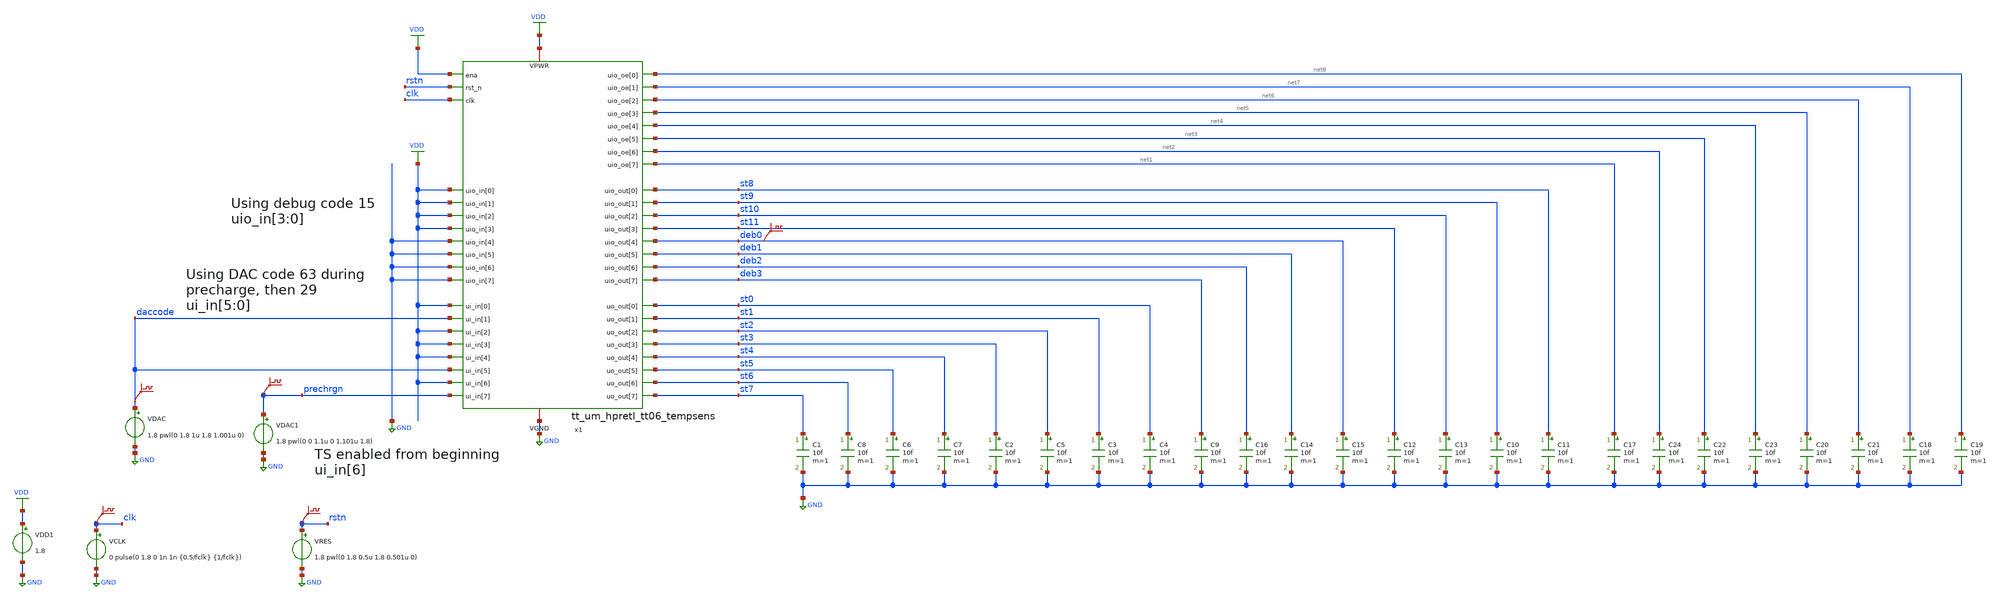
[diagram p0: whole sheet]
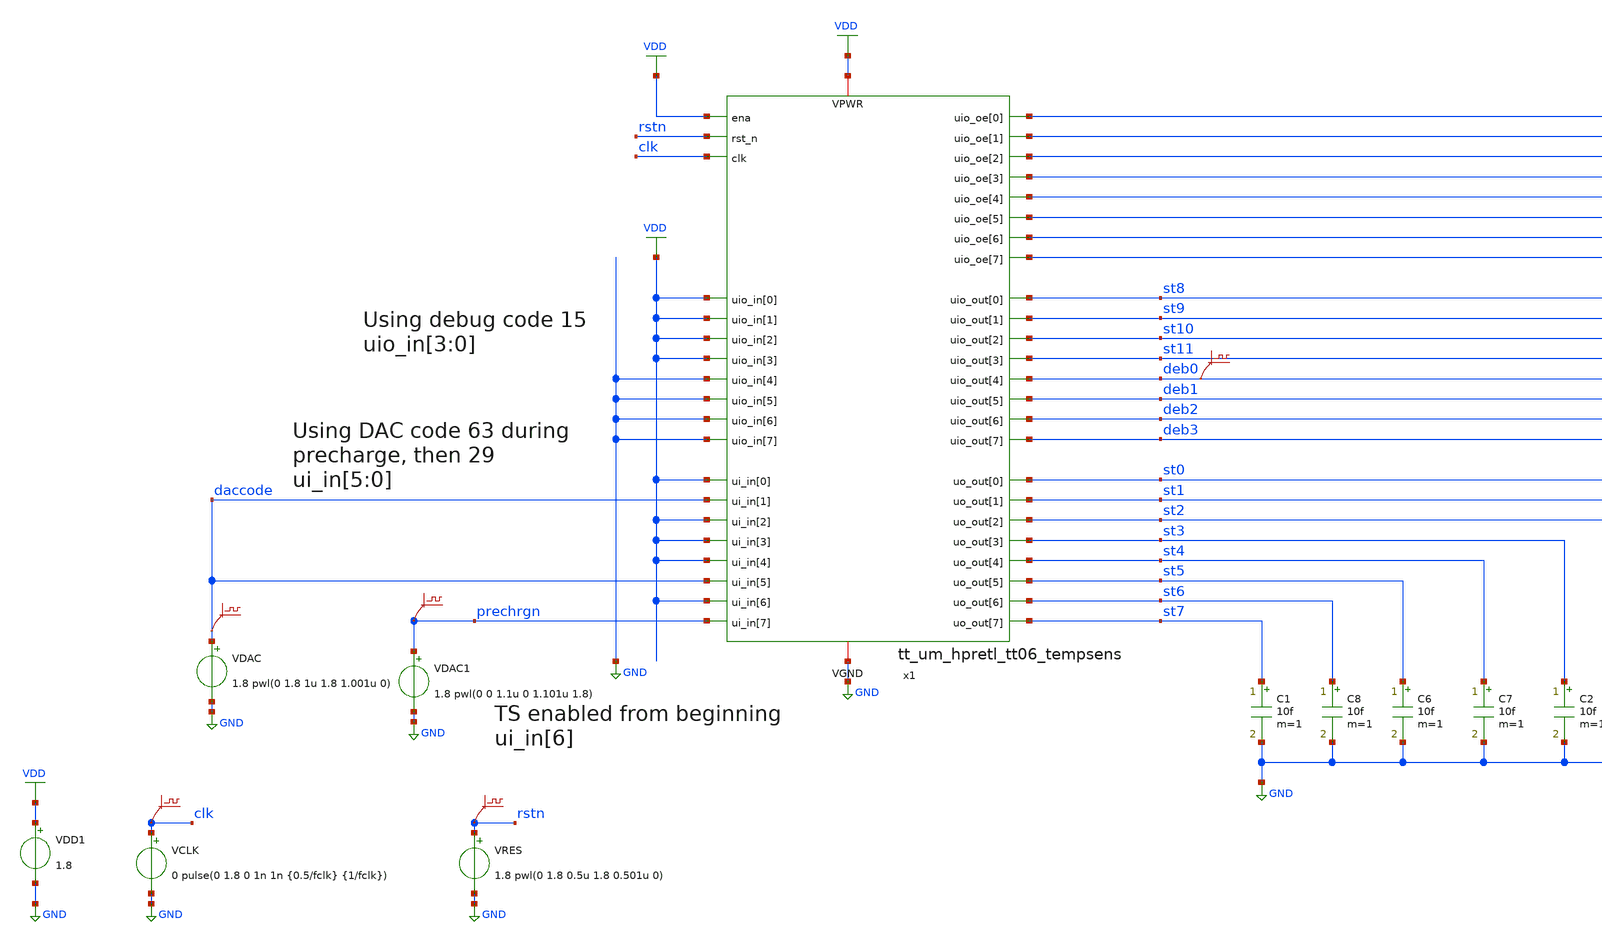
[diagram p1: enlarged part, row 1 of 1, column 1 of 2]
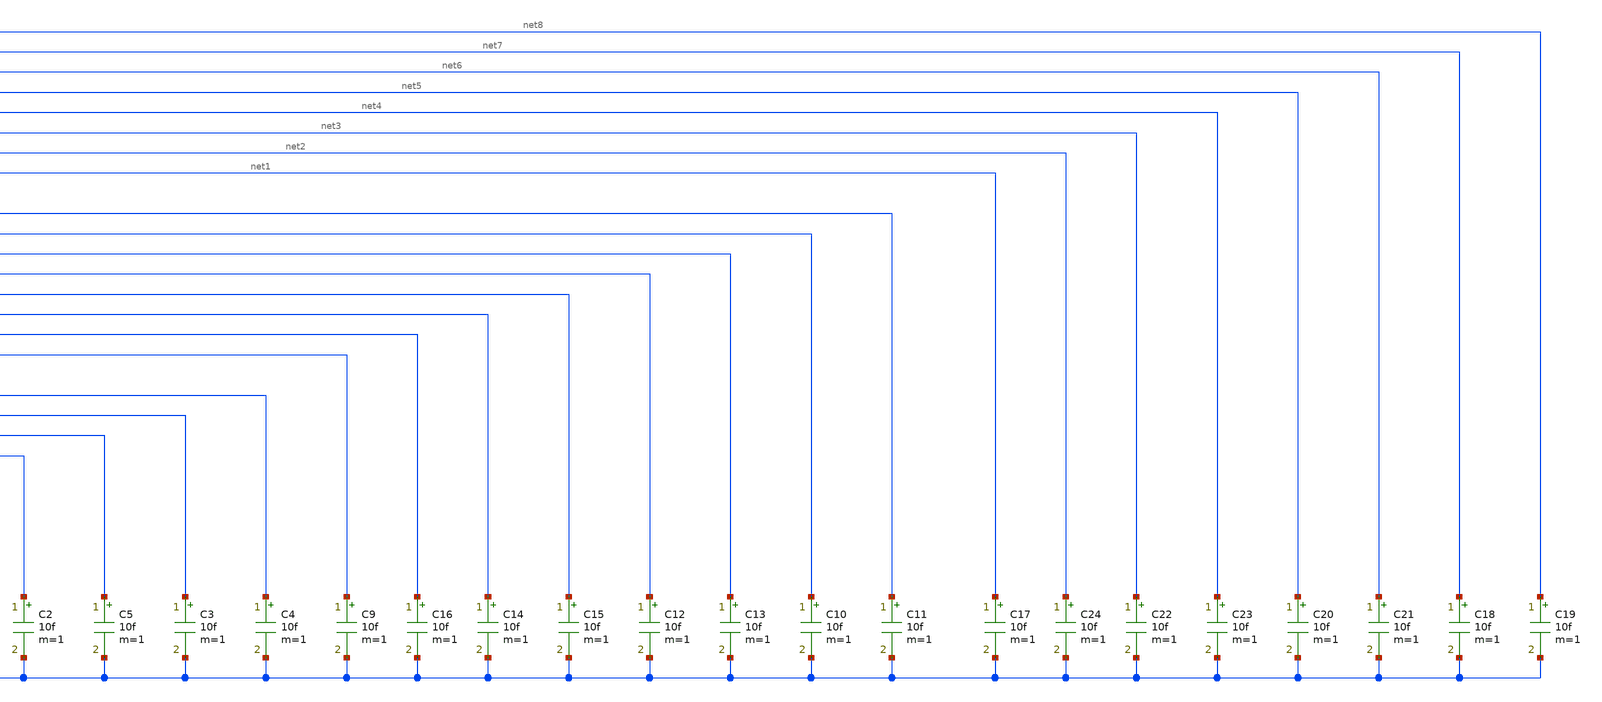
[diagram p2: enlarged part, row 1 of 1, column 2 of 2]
** sch_path: sim/tb_tt06_tempsens.sch
**.subckt tb_tt06_tempsens
VDD1 VDD GND 1.8
VCLK clk GND 0 pulse(0 1.8 0 1n 1n {0.5/fclk} {1/fclk})
VRES rstn GND 1.8 pwl(0 1.8 0.5u 1.8 0.501u 0)
x1 rstn VDD clk VDD daccode VDD VDD VDD daccode VDD prechrgn st0 st1 st2 st3 st4 st5 st6 st7 VDD VDD
+ VDD VDD GND GND GND GND st8 st9 st10 st11 deb0 deb1 deb2 deb3 net8 net7 net6 net5 net4 net3 net2 net1
+ VDD GND tt_um_hpretl_tt06_tempsens
C1 st7 GND 10f m=1
C3 st1 GND 10f m=1
C4 st0 GND 10f m=1
C2 st3 GND 10f m=1
C5 st2 GND 10f m=1
C6 st5 GND 10f m=1
C7 st4 GND 10f m=1
C8 st6 GND 10f m=1
C9 deb3 GND 10f m=1
C10 st9 GND 10f m=1
C11 st8 GND 10f m=1
C12 st11 GND 10f m=1
C13 st10 GND 10f m=1
C14 deb1 GND 10f m=1
C15 deb0 GND 10f m=1
C16 deb2 GND 10f m=1
C17 net1 GND 10f m=1
C18 net7 GND 10f m=1
C19 net8 GND 10f m=1
C20 net5 GND 10f m=1
C21 net6 GND 10f m=1
C22 net3 GND 10f m=1
C23 net4 GND 10f m=1
C24 net2 GND 10f m=1
.save v(deb0)
.save v(rstn)
.save v(clk)
VDAC daccode GND 1.8 pwl(0 1.8 1u 1.8 1.001u 0)
.save v(daccode)
VDAC1 prechrgn GND 1.8 pwl(0 0 1.1u 0 1.101u 1.8)
.save v(prechrgn)
**** begin user architecture code



* ngspice commands
****************

****************
* Misc
****************
.param fclk=10MEG
.options method=gear maxord=2
.temp 30

.save x1.ts.ts_core.dac_vout_ana_
.save x1.ts.ts_core.dcdel_capnode_ana_

.control
set num_threads=6
tran 5u 250u

*exit
.endc




** opencircuitdesign pdks install
.lib $::SKYWATER_MODELS/sky130.lib.spice tt


**** end user architecture code
**.ends

* expanding   symbol:  tt_um_hpretl_tt06_tempsens.sym # of pins=45
** sym_path: sim/tt_um_hpretl_tt06_tempsens.sym
.include tt_um_hpretl_tt06_tempsens.pex.spice
.GLOBAL VDD
.GLOBAL GND
.end
